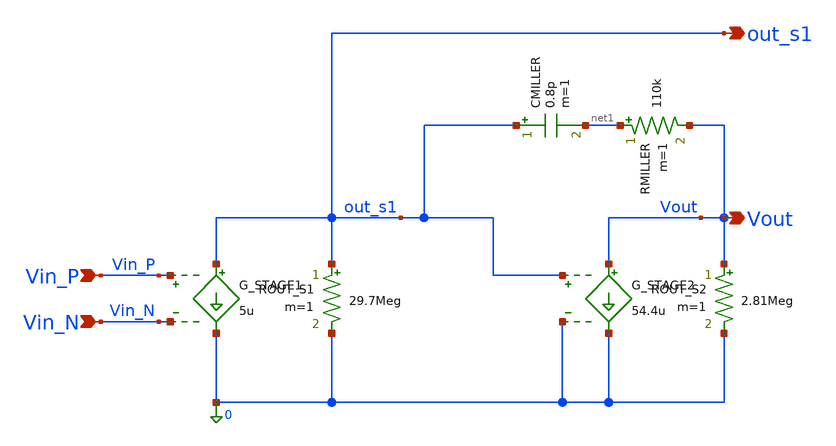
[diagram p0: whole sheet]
** sch_path: dfii/project_2stage_OTA/ota_2stage_ideal.sch
**.subckt ota_2stage_ideal Vin_P Vin_N out_s1 Vout
*.ipin Vin_P
*.ipin Vin_N
*.opin out_s1
*.opin Vout
G_STAGE1 out_s1 0 Vin_P Vin_N 5u
G_STAGE2 Vout 0 out_s1 0 54.4u
ROUT_S1 out_s1 0 29.7Meg m=1
ROUT_S2 Vout 0 2.81Meg m=1
CMILLER out_s1 net1 0.8p m=1
RMILLER net1 Vout 110k m=1
**.ends
.end
